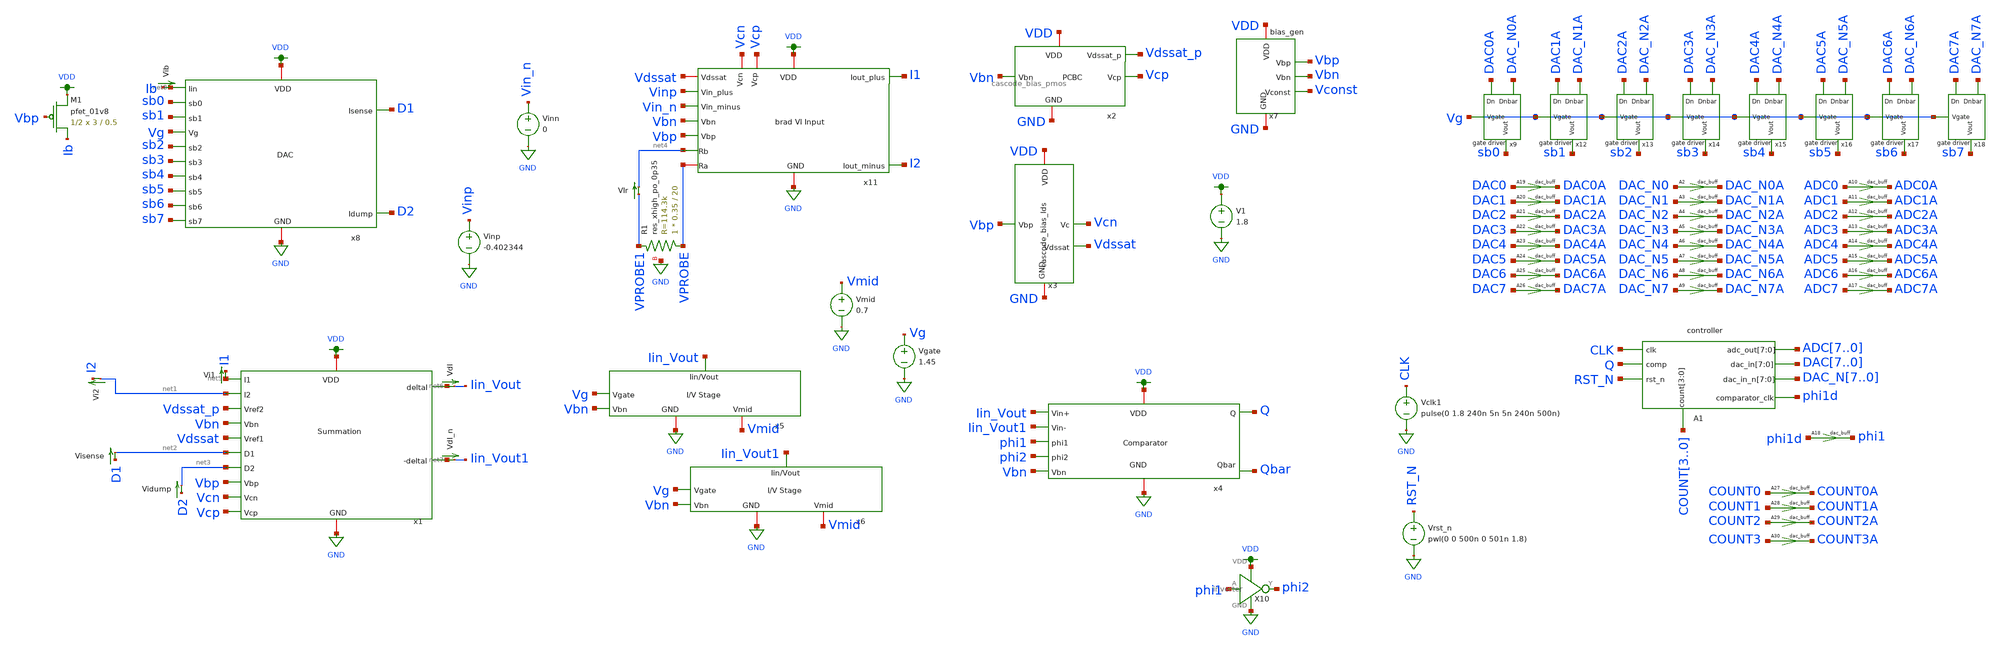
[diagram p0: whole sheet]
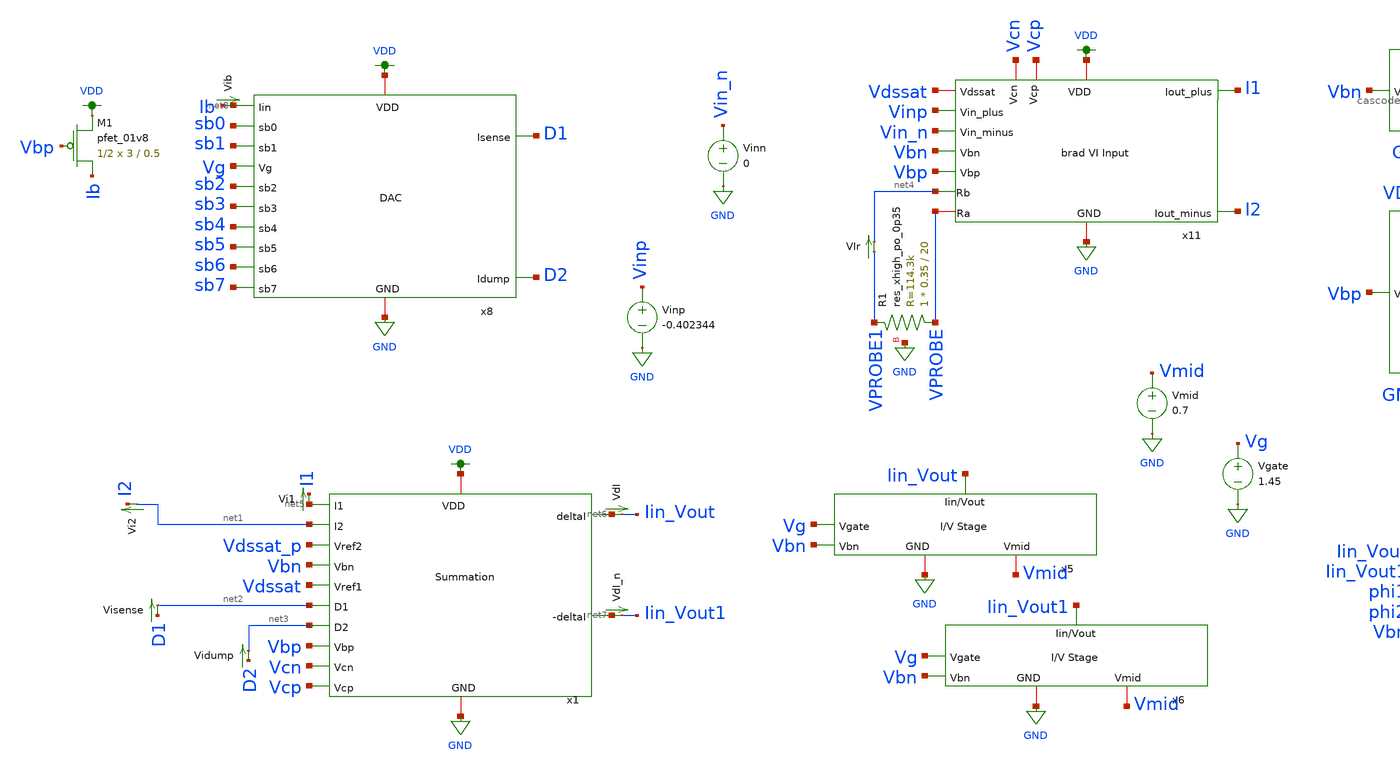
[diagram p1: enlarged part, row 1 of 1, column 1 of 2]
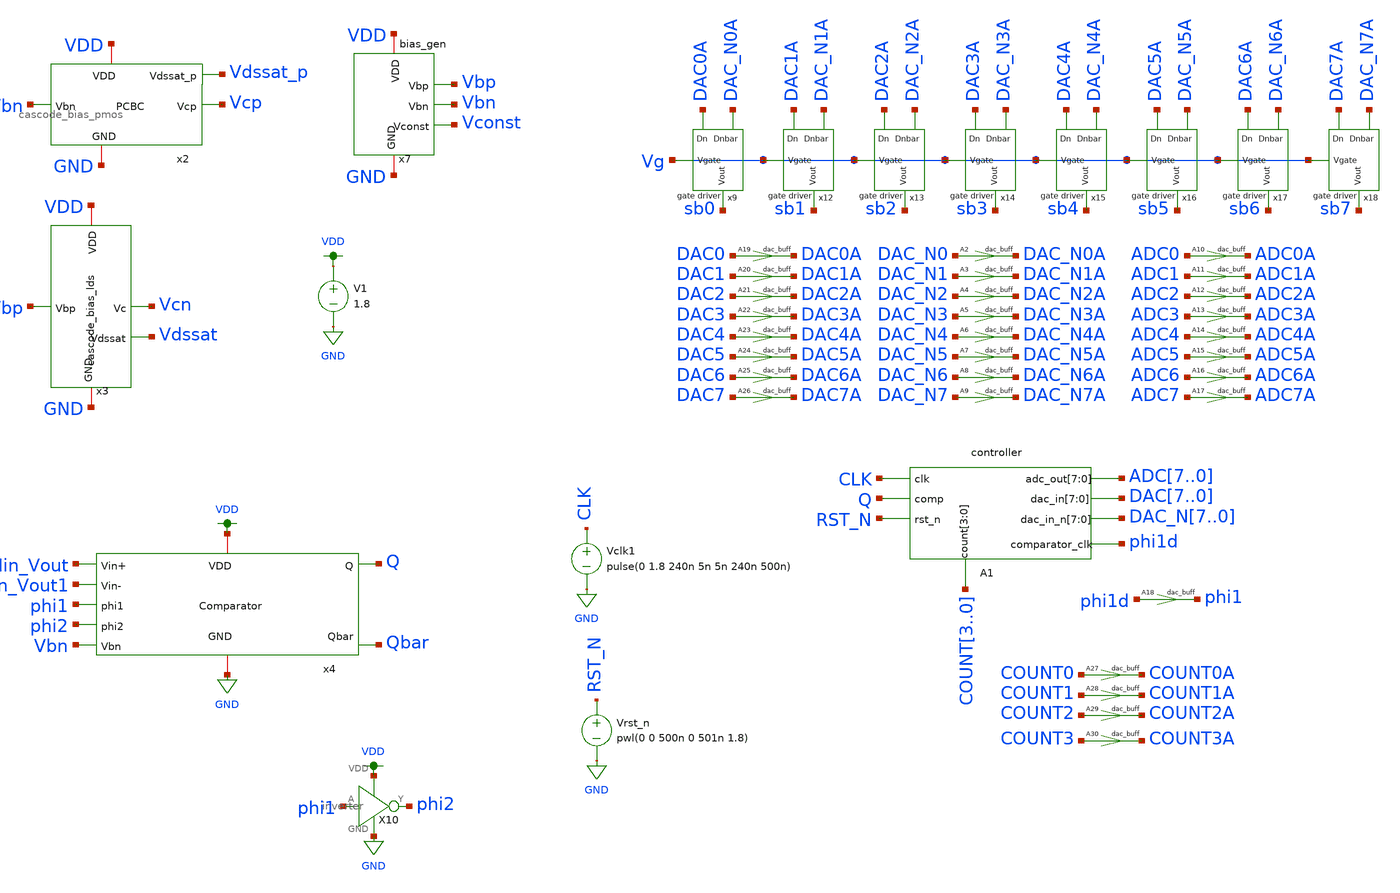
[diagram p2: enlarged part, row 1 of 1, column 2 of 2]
** sch_path: final/schematics/adc_tb_2.sch
**.subckt adc_tb_2
x1 VDD GND net5 net1 Vdssat_p Vbn Vdssat net2 net3 net6 net7 Vbp Vcn Vcp summation
x2 Vbn VDD GND Vcp Vdssat_p cascode_bias_pmos
x3 Vbp VDD Vcn GND Vdssat cascode_bias_lds
V1 VDD GND 1.8
x5 Iin_Vout Vg Vmid Vbn GND IV_converter
x6 Iin_Vout1 Vg Vmid Vbn GND IV_converter
x7 VDD Vbp Vconst GND Vbn bias_gen
Vidump D2 net3 0
.save i(vidump)
Visense D1 net2 0
.save i(visense)
Vi2 net1 I2 0
.save i(vi2)
Vi1 net5 I1 0
.save i(vi1)
x4 VDD Vbn Iin_Vout Iin_Vout1 phi1 phi2 Q Qbar GND comparator
X10 VDD phi1 phi2 GND inverter
x8 sb0 VDD GND sb1 Vg sb2 sb3 D1 sb4 D2 sb5 sb6 sb7 net8 dac
XM1 Ib Vbp VDD VDD sky130_fd_pr__pfet_01v8 L=0.5 W=3 nf=1 ad='int((nf+1)/2) * W/nf * 0.29' as='int((nf+2)/2) * W/nf * 0.29'
+ pd='2*int((nf+1)/2) * (W/nf + 0.29)' ps='2*int((nf+2)/2) * (W/nf + 0.29)' nrd='0.29 / W' nrs='0.29 / W'
+ sa=0 sb=0 sd=0 mult=1/2 m=1/2
Vib Ib net8 0
.save i(vib)
Vinp Vinp GND -0.402344
Vinn Vin_n GND 0
x11 VDD I1 I2 Vinp Vin_n Vbn Vbp Vcn GND VPROBE net4 Vdssat Vcp brad_VI_input
VIr VPROBE1 net4 0
.save i(vir)
XR1 VPROBE VPROBE1 GND sky130_fd_pr__res_xhigh_po_0p35 L=20 mult=1 m=1
VdI net6 Iin_Vout 0
.save i(vdi)
VdI_n net7 Iin_Vout1 0
.save i(vdi_n)
Vclk1 CLK GND pulse(0 1.8 240n 5n 5n 240n 500n)
Vrst_n RST_N GND pwl(0 0 500n 0 501n 1.8)
A2 [ DAC_N0 ] [ DAC_N0A ] dac_buff
A3 [ DAC_N1 ] [ DAC_N1A ] dac_buff
A4 [ DAC_N2 ] [ DAC_N2A ] dac_buff
A5 [ DAC_N3 ] [ DAC_N3A ] dac_buff
A6 [ DAC_N4 ] [ DAC_N4A ] dac_buff
A7 [ DAC_N5 ] [ DAC_N5A ] dac_buff
A8 [ DAC_N6 ] [ DAC_N6A ] dac_buff
A9 [ DAC_N7 ] [ DAC_N7A ] dac_buff
A1 [ CLK Q RST_N ] [ DAC7 DAC6 DAC5 DAC4 DAC3 DAC2 DAC1 DAC0 DAC_N7 DAC_N6 DAC_N5 DAC_N4 DAC_N3
+ DAC_N2 DAC_N1 DAC_N0 phi1d ADC7 ADC6 ADC5 ADC4 ADC3 ADC2 ADC1 ADC0 COUNT3 COUNT2 COUNT1 COUNT0 ] null
+ controller
.model controller d_cosim
+ simulation="../../Documents/madvlsi/final/schematics/controller/librelane/controller.so"
A10 [ ADC0 ] [ ADC0A ] dac_buff
A11 [ ADC1 ] [ ADC1A ] dac_buff
A12 [ ADC2 ] [ ADC2A ] dac_buff
A13 [ ADC3 ] [ ADC3A ] dac_buff
A14 [ ADC4 ] [ ADC4A ] dac_buff
A15 [ ADC5 ] [ ADC5A ] dac_buff
A16 [ ADC6 ] [ ADC6A ] dac_buff
A17 [ ADC7 ] [ ADC7A ] dac_buff
A18 [ phi1d ] [ phi1 ] dac_buff
x9 Vg DAC0A sb0 DAC_N0A gate_driver
A19 [ DAC0 ] [ DAC0A ] dac_buff
A20 [ DAC1 ] [ DAC1A ] dac_buff
A21 [ DAC2 ] [ DAC2A ] dac_buff
A22 [ DAC3 ] [ DAC3A ] dac_buff
A23 [ DAC4 ] [ DAC4A ] dac_buff
A24 [ DAC5 ] [ DAC5A ] dac_buff
A25 [ DAC6 ] [ DAC6A ] dac_buff
A26 [ DAC7 ] [ DAC7A ] dac_buff
x12 Vg DAC1A sb1 DAC_N1A gate_driver
x13 Vg DAC2A sb2 DAC_N2A gate_driver
x14 Vg DAC3A sb3 DAC_N3A gate_driver
x15 Vg DAC4A sb4 DAC_N4A gate_driver
x16 Vg DAC5A sb5 DAC_N5A gate_driver
x17 Vg DAC6A sb6 DAC_N6A gate_driver
x18 Vg DAC7A sb7 DAC_N7A gate_driver
A27 [ COUNT0 ] [ COUNT0A ] dac_buff
A28 [ COUNT1 ] [ COUNT1A ] dac_buff
A29 [ COUNT2 ] [ COUNT2A ] dac_buff
A30 [ COUNT3 ] [ COUNT3A ] dac_buff
Vgate Vg GND 1.45
Vmid Vmid GND 0.7
**** begin user architecture code
.lib $::SKYWATER_MODELS/sky130.lib.spice tt


.control
  save all
  set wr_vecnames
  set wr_singlescale
  remzerovec
  tran 2n 9000n
  * write adc_tb_2.raw
  wrdata ~/Documents/madvlsi/final/schematics/adctest/adc_tb2.txt v(rst_n) v(vinp) v(sb0) v(sb1)
+ v(sb2) v(sb3) v(sb4) v(sb5) v(sb6) v(sb7) v(adc0a) v(adc1a) v(adc2a) v(adc3a) v(adc4a) v(adc5a) v(adc6a)
+ v(adc7a) v(count0a) v(count1a) v(count2a) v(count3a)
  quit
.endc


**** end user architecture code
**.ends
.GLOBAL VDD
.GLOBAL GND
**** begin user architecture code
.model dac_buff dac_bridge input_load=1e-15 t_rise=1n t_fall=1n  out_low=0 out_high=1.8
**** end user architecture code
.end
